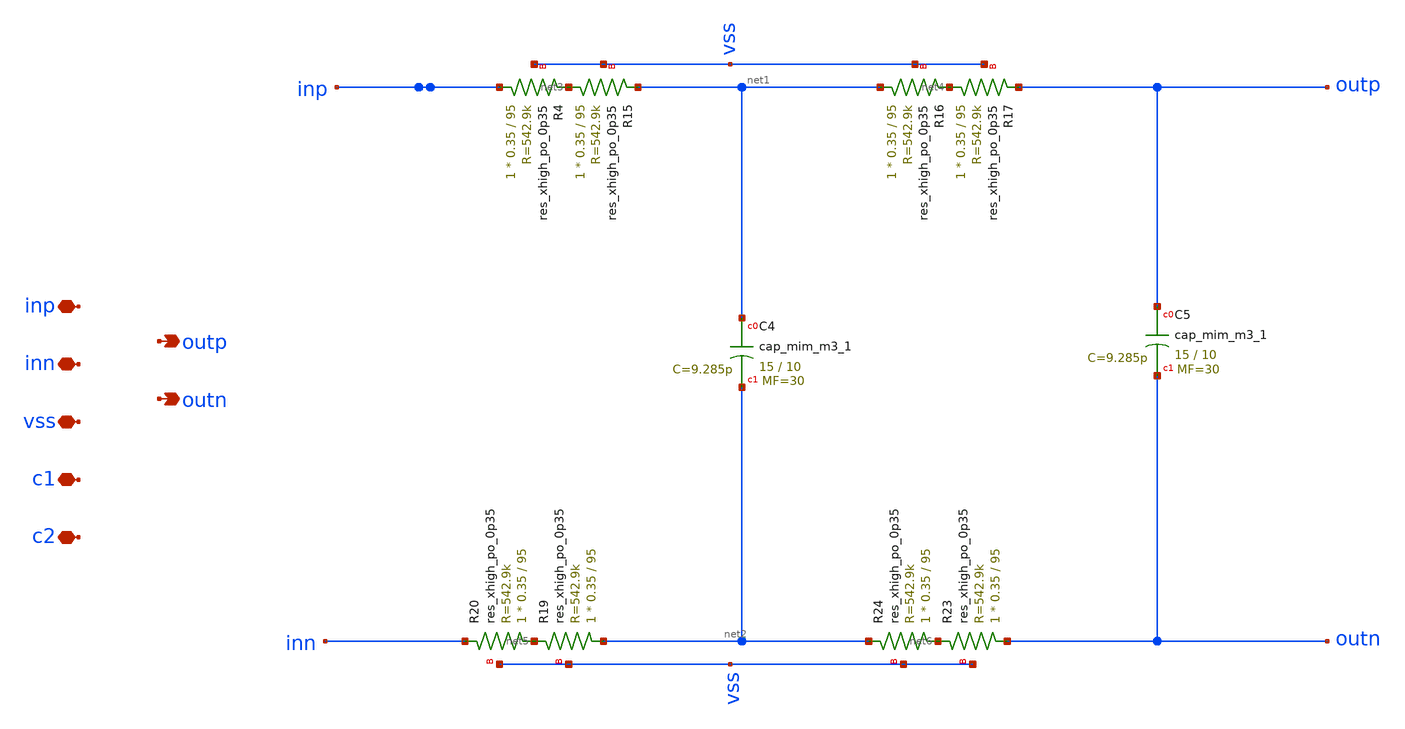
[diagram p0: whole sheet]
** sch_path: AAFilter.sch
**.subckt AAFilter inp inn vss outp outn c1 c2
*.iopin inp
*.iopin inn
*.iopin vss
*.opin outp
*.opin outn
*.iopin c1
*.iopin c2
XR4 inp net3 vss sky130_fd_pr__res_xhigh_po_0p35 L=95 mult=1 m=1
XR15 net3 net1 vss sky130_fd_pr__res_xhigh_po_0p35 L=95 mult=1 m=1
XR16 net1 net4 vss sky130_fd_pr__res_xhigh_po_0p35 L=95 mult=1 m=1
XR17 net4 outp vss sky130_fd_pr__res_xhigh_po_0p35 L=95 mult=1 m=1
XR19 net2 net5 vss sky130_fd_pr__res_xhigh_po_0p35 L=95 mult=1 m=1
XR20 net5 inn vss sky130_fd_pr__res_xhigh_po_0p35 L=95 mult=1 m=1
XR23 outn net6 vss sky130_fd_pr__res_xhigh_po_0p35 L=95 mult=1 m=1
XR24 net6 net2 vss sky130_fd_pr__res_xhigh_po_0p35 L=95 mult=1 m=1
XC4 net1 net2 sky130_fd_pr__cap_mim_m3_1 W=15 L=10 MF=30 m=30
XC5 outp outn sky130_fd_pr__cap_mim_m3_1 W=15 L=10 MF=30 m=30
**.ends
.end
